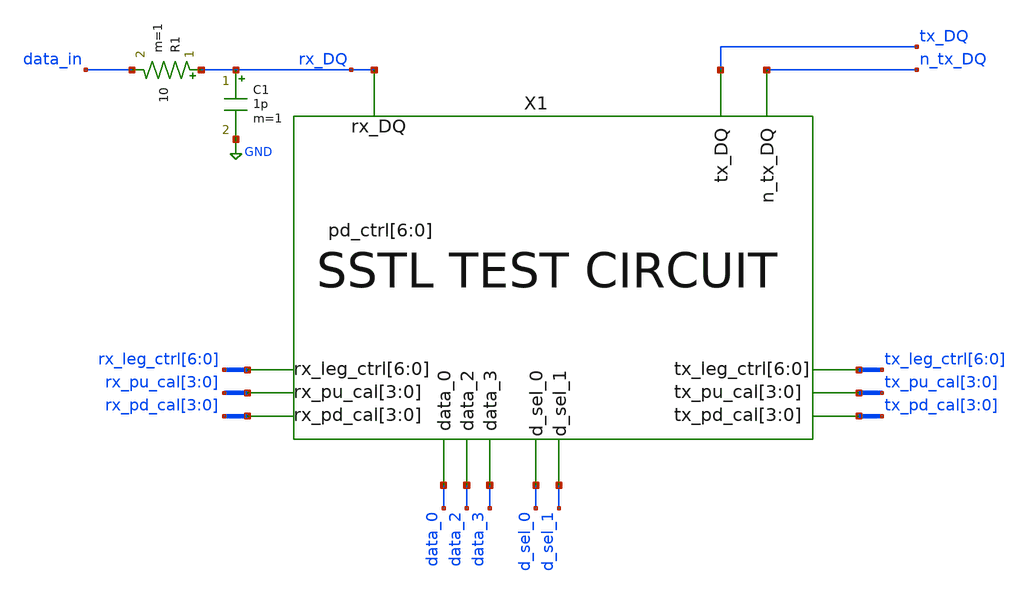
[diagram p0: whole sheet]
** sch_path: xschem/proj_sstl_test_tb.sch
* Copyright 2021 Stefan Frederik Schippers
* Licensed under the Apache License, Version 2.0 (the "License");
* you may not use this file except in compliance with the License.
* You may obtain a copy of the License at
* https://www.apache.org/licenses/LICENSE-2.0
* Unless required by applicable law or agreed to in writing, software
* distributed under the License is distributed on an "AS IS" BASIS,
* WITHOUT WARRANTIES OR CONDITIONS OF ANY KIND, either express or implied.
* See the License for the specific language governing permissions and
* limitations under the License.
**.subckt proj_sstl_test_tb
X1 rx_leg_ctrl[6] rx_leg_ctrl[5] rx_leg_ctrl[4] rx_leg_ctrl[3] rx_leg_ctrl[2] rx_leg_ctrl[1]
+ rx_leg_ctrl[0] rx_pu_cal[3] rx_pu_cal[2] rx_pu_cal[1] rx_pu_cal[0] rx_pd_cal[3] rx_pd_cal[2] rx_pd_cal[1]
+ rx_pd_cal[0] tx_leg_ctrl[6] tx_leg_ctrl[5] tx_leg_ctrl[4] tx_leg_ctrl[3] tx_leg_ctrl[2] tx_leg_ctrl[1]
+ tx_leg_ctrl[0] tx_pu_cal[3] tx_pu_cal[2] tx_pu_cal[1] tx_pu_cal[0] tx_pd_cal[3] tx_pd_cal[2] tx_pd_cal[1]
+ tx_pd_cal[0] data_0 data_2 data_3 d_sel_0 d_sel_1 rx_DQ tx_DQ n_tx_DQ VDD IOVDD GND proj_sstl_test
C1 rx_DQ GND 1p m=1
R1 rx_DQ data_in 10 m=1
**** begin user architecture code
 ** Local library links to pdk
.lib ./sky130/libs/tt_lib.spice tt
.include $::SKYWATER_STDCELLS/sky130_fd_sc_hd.spice

**** end user architecture code
**.ends
.GLOBAL GND
**** begin user architecture code


* power voltage
vvdd VDD 0 1.5

** STATIC CONTOL
vrx_leg_ctrl[0] rx_leg_ctrl[0] VDD 0
vrx_leg_ctrl[1] rx_leg_ctrl[1] VDD 0
vrx_leg_ctrl[2] rx_leg_ctrl[2] VDD 0
vrx_leg_ctrl[3] rx_leg_ctrl[3]  0  0
vrx_leg_ctrl[4] rx_leg_ctrl[4]  0  0
vrx_leg_ctrl[5] rx_leg_ctrl[5]  0  0
vrx_leg_ctrl[6] rx_leg_ctrl[6]  0  0

vtx_leg_ctrl[0] tx_leg_ctrl[0] VDD 0
vtx_leg_ctrl[1] tx_leg_ctrl[1] VDD 0
vtx_leg_ctrl[2] tx_leg_ctrl[2] VDD 0
vtx_leg_ctrl[3] tx_leg_ctrl[3] VDD 0
vtx_leg_ctrl[4] tx_leg_ctrl[4] VDD 0
vtx_leg_ctrl[5] tx_leg_ctrl[5] VDD 0
vtx_leg_ctrl[6] tx_leg_ctrl[6] VDD 0

vtx_pu_cal[3] tx_pu_cal[3]  0  0
vtx_pu_cal[2] tx_pu_cal[2] VDD 0
vtx_pu_cal[1] tx_pu_cal[1] VDD 0
vtx_pu_cal[0] tx_pu_cal[0] VDD 0

vtx_pd_cal[3] tx_pd_cal[3]  0  0
vtx_pd_cal[2] tx_pd_cal[2] VDD 0
vtx_pd_cal[1] tx_pd_cal[1] VDD 0
vtx_pd_cal[0] tx_pd_cal[0] VDD 0

vrx_pu_cal[3] rx_pu_cal[3]  0  0
vrx_pu_cal[2] rx_pu_cal[2] VDD 0
vrx_pu_cal[1] rx_pu_cal[1] VDD 0
vrx_pu_cal[0] rx_pu_cal[0] VDD 0

vrx_pd_cal[3] rx_pd_cal[3]  0  0
vrx_pd_cal[2] rx_pd_cal[2] VDD 0
vrx_pd_cal[1] rx_pd_cal[1] VDD 0
vrx_pd_cal[0] rx_pd_cal[0] VDD 0

vd0 data_0  0  0
vd2 data_2 VDD 0
vd3 data_3  0  0

vs1 d_sel_1  0  0
vs0 d_sel_0 VDD 0


** Signal
*                                vlow, vhigh, delay, risetime, falltime, pulsewidth, period, phase
* vpu_ctrl0 pu_ctrl[0] 0 0 PULSE 0   SED_puctrl0_SED 1n 10p 10p 5n 10n 0
vsig data_in 0 0 PULSE 0 1.5 1n 10p 10p 5n 10n 0


.control
save all
set temp=27

* RUN SIMULATION
tran 1p 8n

* OUTPUT
set hcopydevtype = svg
hardcopy ./sstl_test_proj.svg   rx_DQ tx_DQ n_tx_DQ title 'SSTL Test Circuit'
hardcopy ./sstl_test_proj_2.svg rx_DQ x1.d_out       title 'SSTL Test Circuit'

.endc


**** end user architecture code
.end
